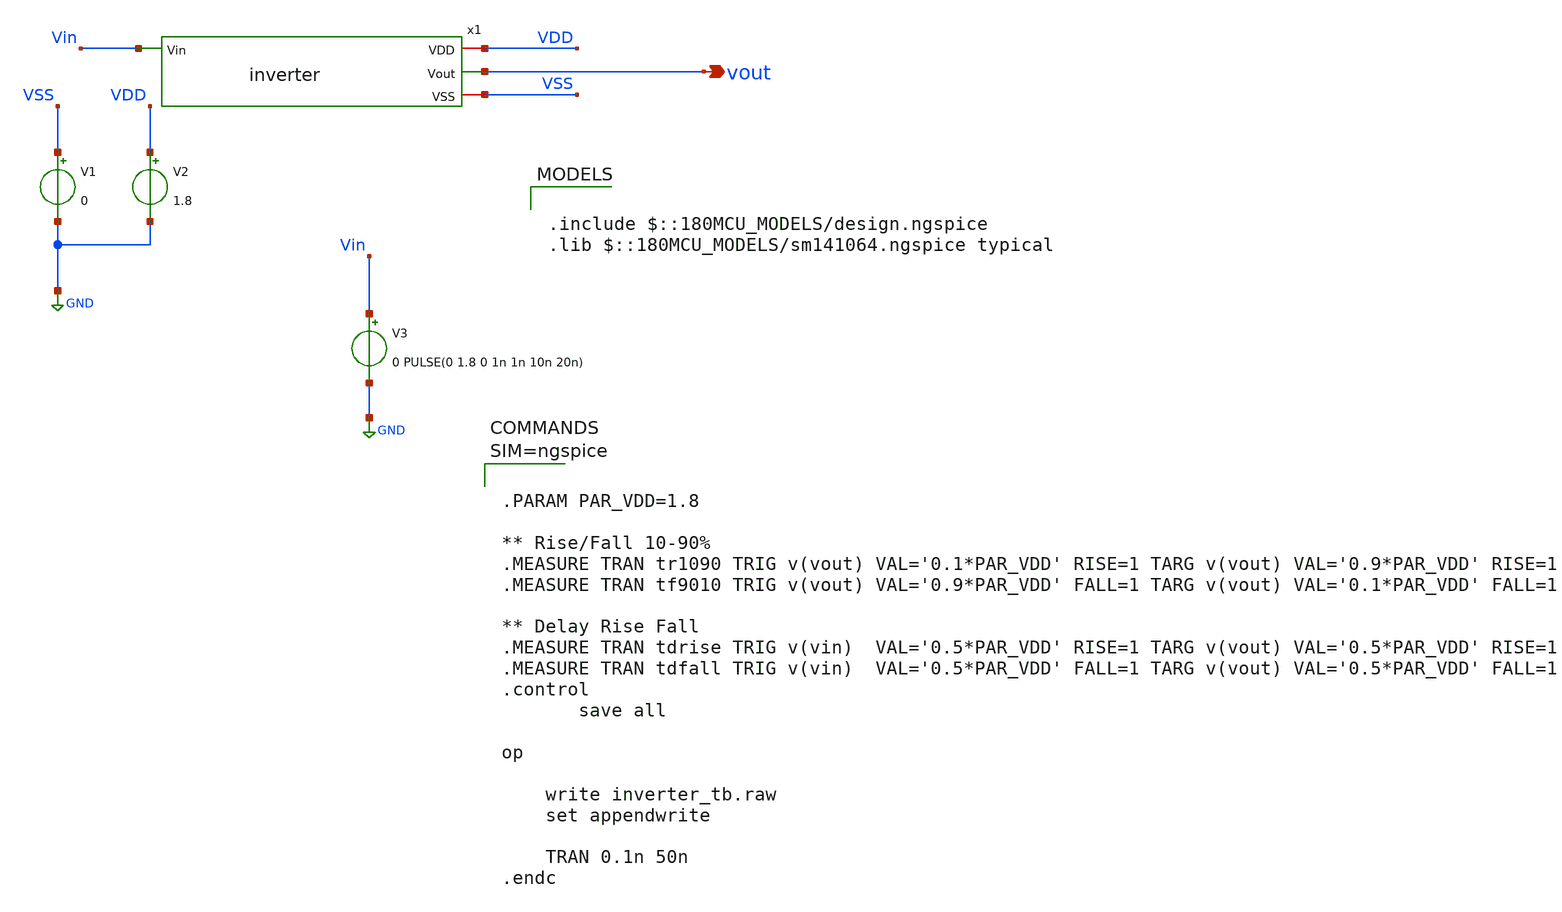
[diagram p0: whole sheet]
** sch_path: xschem/inverter_tb.sch
**.subckt inverter_tb vout
*.opin vout
V1 VSS GND 0
V2 VDD GND 1.8
V3 Vin GND 0 PULSE(0 1.8 0 1n 1n 10n 20n)
x1 VDD vout Vin VSS inverter
**** begin user architecture code

.include $::180MCU_MODELS/design.ngspice
.lib $::180MCU_MODELS/sm141064.ngspice typical




.PARAM PAR_VDD=1.8

** Rise/Fall 10-90%
.MEASURE TRAN tr1090 TRIG v(vout) VAL='0.1*PAR_VDD' RISE=1 TARG v(vout) VAL='0.9*PAR_VDD' RISE=1
.MEASURE TRAN tf9010 TRIG v(vout) VAL='0.9*PAR_VDD' FALL=1 TARG v(vout) VAL='0.1*PAR_VDD' FALL=1

** Delay Rise Fall
.MEASURE TRAN tdrise TRIG v(vin)  VAL='0.5*PAR_VDD' RISE=1 TARG v(vout) VAL='0.5*PAR_VDD' RISE=1
.MEASURE TRAN tdfall TRIG v(vin)  VAL='0.5*PAR_VDD' FALL=1 TARG v(vout) VAL='0.5*PAR_VDD' FALL=1
.control
	   save all

op

    write inverter_tb.raw
    set appendwrite

	TRAN 0.1n 50n
.endc




**** end user architecture code
**.ends

* expanding   symbol:  inverter.sym # of pins=4
** sym_path: xschem/inverter.sym
** sch_path: xschem/inverter.sch
.subckt inverter VDD Vout Vin VSS
*.opin Vout
*.iopin VDD
*.iopin VSS
*.ipin Vin
XM3 Vout Vin VSS VSS nfet_03v3 L=0.28u W=0.22u nf=1 ad='int((nf+1)/2) * W/nf * 0.18u' as='int((nf+2)/2) * W/nf * 0.18u'
+ pd='2*int((nf+1)/2) * (W/nf + 0.18u)' ps='2*int((nf+2)/2) * (W/nf + 0.18u)' nrd='0.18u / W' nrs='0.18u / W'
+ sa=0 sb=0 sd=0 m=1
XM2 Vout Vin VDD VDD pfet_03v3 L=0.28u W=0.44u nf=1 ad='int((nf+1)/2) * W/nf * 0.18u' as='int((nf+2)/2) * W/nf * 0.18u'
+ pd='2*int((nf+1)/2) * (W/nf + 0.18u)' ps='2*int((nf+2)/2) * (W/nf + 0.18u)' nrd='0.18u / W' nrs='0.18u / W'
+ sa=0 sb=0 sd=0 m=1
.ends

.GLOBAL GND
.end
